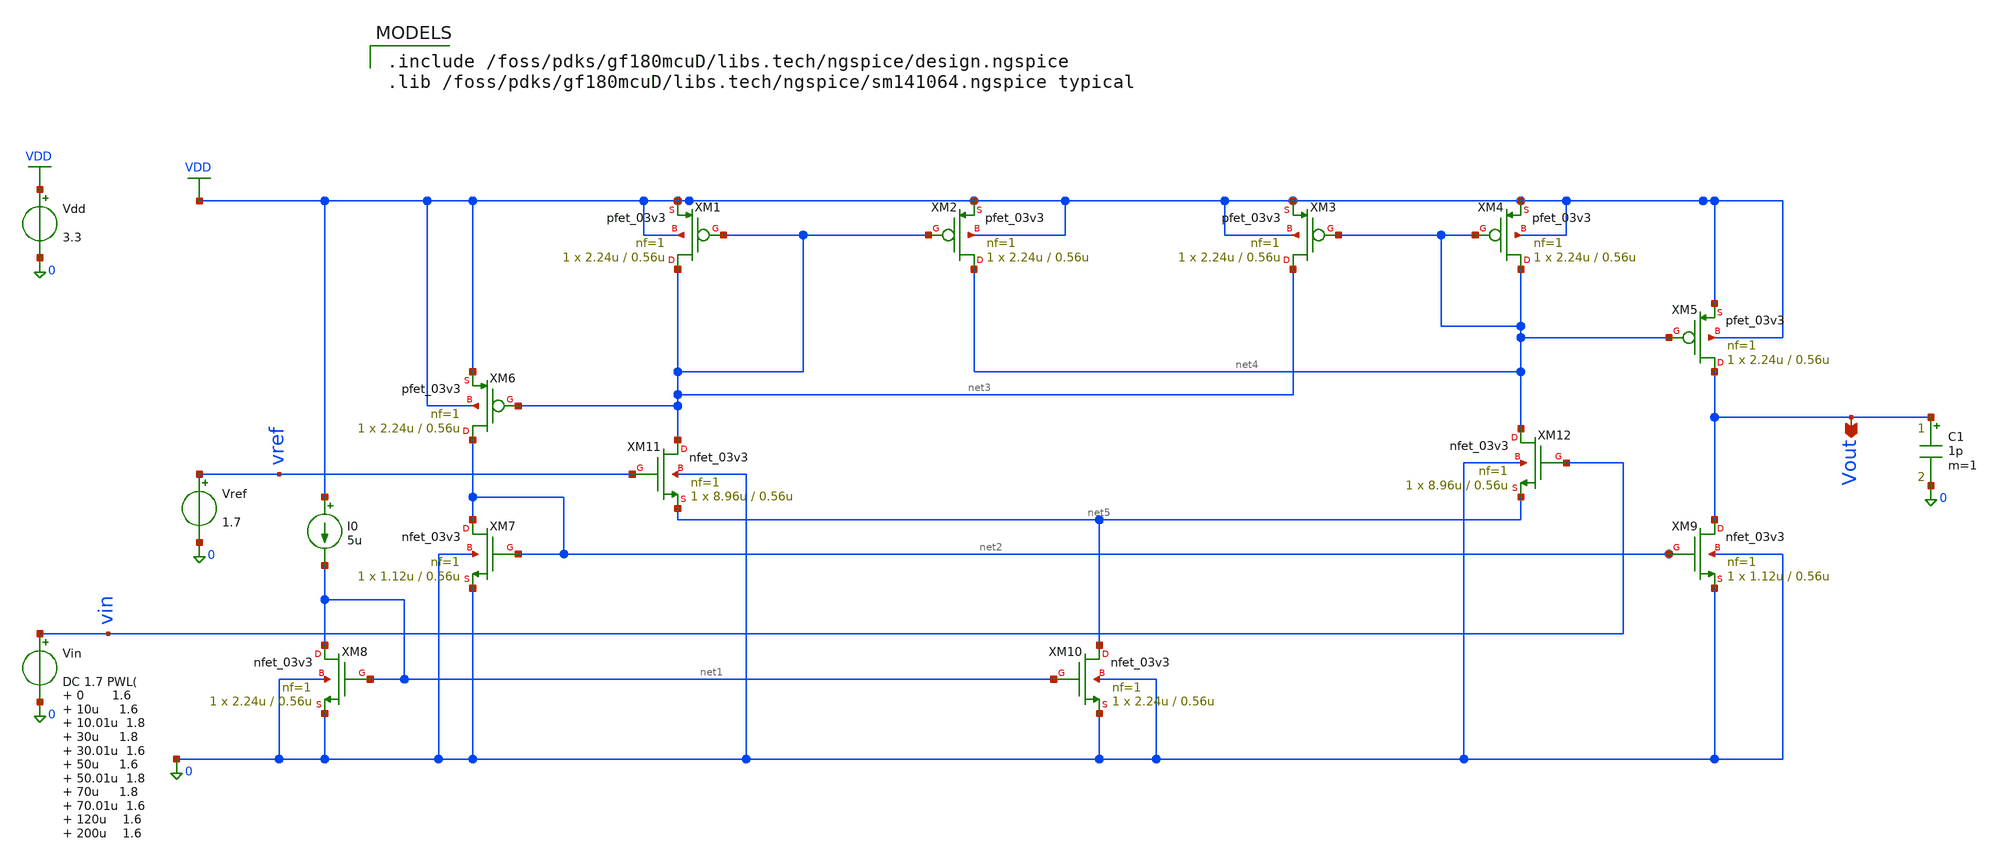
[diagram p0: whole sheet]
** sch_path: comparator/schematic-design/comparator_plot.sch
**.subckt comparator_plot Vout
*.opin Vout
XM1 net3 net3 VDD VDD pfet_03v3 L=0.56u W=2.24u nf=1 ad='int((nf+1)/2) * W/nf * 0.18u' as='int((nf+2)/2) * W/nf * 0.18u'
+ pd='2*int((nf+1)/2) * (W/nf + 0.18u)' ps='2*int((nf+2)/2) * (W/nf + 0.18u)' nrd='0.18u / W' nrs='0.18u / W'
+ sa=0 sb=0 sd=0 m=1
XM2 net4 net3 VDD VDD pfet_03v3 L=0.56u W=2.24u nf=1 ad='int((nf+1)/2) * W/nf * 0.18u' as='int((nf+2)/2) * W/nf * 0.18u'
+ pd='2*int((nf+1)/2) * (W/nf + 0.18u)' ps='2*int((nf+2)/2) * (W/nf + 0.18u)' nrd='0.18u / W' nrs='0.18u / W'
+ sa=0 sb=0 sd=0 m=1
XM3 net3 net4 VDD VDD pfet_03v3 L=0.56u W=2.24u nf=1 ad='int((nf+1)/2) * W/nf * 0.18u' as='int((nf+2)/2) * W/nf * 0.18u'
+ pd='2*int((nf+1)/2) * (W/nf + 0.18u)' ps='2*int((nf+2)/2) * (W/nf + 0.18u)' nrd='0.18u / W' nrs='0.18u / W'
+ sa=0 sb=0 sd=0 m=1
XM4 net4 net4 VDD VDD pfet_03v3 L=0.56u W=2.24u nf=1 ad='int((nf+1)/2) * W/nf * 0.18u' as='int((nf+2)/2) * W/nf * 0.18u'
+ pd='2*int((nf+1)/2) * (W/nf + 0.18u)' ps='2*int((nf+2)/2) * (W/nf + 0.18u)' nrd='0.18u / W' nrs='0.18u / W'
+ sa=0 sb=0 sd=0 m=1
XM5 Vout net4 VDD VDD pfet_03v3 L=0.56u W=2.24u nf=1 ad='int((nf+1)/2) * W/nf * 0.18u' as='int((nf+2)/2) * W/nf * 0.18u'
+ pd='2*int((nf+1)/2) * (W/nf + 0.18u)' ps='2*int((nf+2)/2) * (W/nf + 0.18u)' nrd='0.18u / W' nrs='0.18u / W'
+ sa=0 sb=0 sd=0 m=1
XM6 net2 net3 VDD VDD pfet_03v3 L=0.56u W=2.24u nf=1 ad='int((nf+1)/2) * W/nf * 0.18u' as='int((nf+2)/2) * W/nf * 0.18u'
+ pd='2*int((nf+1)/2) * (W/nf + 0.18u)' ps='2*int((nf+2)/2) * (W/nf + 0.18u)' nrd='0.18u / W' nrs='0.18u / W'
+ sa=0 sb=0 sd=0 m=1
XM7 net2 net2 0 0 nfet_03v3 L=0.56u W=1.12u nf=1 ad='int((nf+1)/2) * W/nf * 0.18u' as='int((nf+2)/2) * W/nf * 0.18u'
+ pd='2*int((nf+1)/2) * (W/nf + 0.18u)' ps='2*int((nf+2)/2) * (W/nf + 0.18u)' nrd='0.18u / W' nrs='0.18u / W'
+ sa=0 sb=0 sd=0 m=1
XM8 net1 net1 0 0 nfet_03v3 L=0.56u W=2.24u nf=1 ad='int((nf+1)/2) * W/nf * 0.18u' as='int((nf+2)/2) * W/nf * 0.18u'
+ pd='2*int((nf+1)/2) * (W/nf + 0.18u)' ps='2*int((nf+2)/2) * (W/nf + 0.18u)' nrd='0.18u / W' nrs='0.18u / W'
+ sa=0 sb=0 sd=0 m=1
XM9 Vout net2 0 0 nfet_03v3 L=0.56u W=1.12u nf=1 ad='int((nf+1)/2) * W/nf * 0.18u' as='int((nf+2)/2) * W/nf * 0.18u'
+ pd='2*int((nf+1)/2) * (W/nf + 0.18u)' ps='2*int((nf+2)/2) * (W/nf + 0.18u)' nrd='0.18u / W' nrs='0.18u / W'
+ sa=0 sb=0 sd=0 m=1
XM10 net5 net1 0 0 nfet_03v3 L=0.56u W=2.24u nf=1 ad='int((nf+1)/2) * W/nf * 0.18u' as='int((nf+2)/2) * W/nf * 0.18u'
+ pd='2*int((nf+1)/2) * (W/nf + 0.18u)' ps='2*int((nf+2)/2) * (W/nf + 0.18u)' nrd='0.18u / W' nrs='0.18u / W'
+ sa=0 sb=0 sd=0 m=1
XM11 net3 vref net5 0 nfet_03v3 L=0.56u W=8.96u nf=1 ad='int((nf+1)/2) * W/nf * 0.18u' as='int((nf+2)/2) * W/nf * 0.18u'
+ pd='2*int((nf+1)/2) * (W/nf + 0.18u)' ps='2*int((nf+2)/2) * (W/nf + 0.18u)' nrd='0.18u / W' nrs='0.18u / W'
+ sa=0 sb=0 sd=0 m=1
XM12 net4 vin net5 0 nfet_03v3 L=0.56u W=8.96u nf=1 ad='int((nf+1)/2) * W/nf * 0.18u' as='int((nf+2)/2) * W/nf * 0.18u'
+ pd='2*int((nf+1)/2) * (W/nf + 0.18u)' ps='2*int((nf+2)/2) * (W/nf + 0.18u)' nrd='0.18u / W' nrs='0.18u / W'
+ sa=0 sb=0 sd=0 m=1
I0 VDD net1 5u
Vref vref 0 1.7
Vin vin 0 DC 1.7 PWL( 0 1.6 10u 1.6 10.01u 1.8 30u 1.8 30.01u 1.6 50u 1.6 50.01u 1.8 70u 1.8 70.01u
+ 1.6 120u 1.6 200u 1.6 300u 1.8 400u 1.6 420u 1.6
)

Vdd VDD 0 3.3
C1 Vout 0 1p m=1
**** begin user architecture code

.include /foss/pdks/gf180mcuD/libs.tech/ngspice/design.ngspice
.lib /foss/pdks/gf180mcuD/libs.tech/ngspice/sm141064.ngspice typical


.control
set noaskquit
save v(vin) v(vref) v(vout) i(Vdd)

* ============================================================
* FIGURE 1 — DC TRANSFER / COMPARATOR SPECIFICATION
* Current design: VDD=3.3 V, VREF=1.7 V
* Sweep VIN around VREF. The output transition gives the trip point.
* ============================================================
set appendwrite
alter @Vin[dc] = 1.7
dc Vin 1.60 1.80 0.1m
meas dc vtrip_up find v(vin) when v(vout)=1.65 rise=1
write comparator_fig1_up.raw v(vin) v(vout)

reset
alter @Vin[dc] = 1.7
dc Vin 1.80 1.60 -0.1m
meas dc vtrip_down find v(vin) when v(vout)=1.65 fall=1
write comparator_fig1_down.raw v(vin) v(vout)

let vhyst_mV = abs(vtrip_up-vtrip_down)*1e3
let vcenter = (vtrip_up+vtrip_down)/2
let center_error_mV = (vcenter-1.7)*1e3
print vtrip_up vtrip_down vhyst_mV vcenter center_error_mV

* Open comparator_fig1_up.raw and comparator_fig1_down.raw together in
* Xschem's graph viewer to reproduce the two switching thresholds.
plot v(vout) vs v(vin) xlimit 1.60 1.80 ylimit -0.1 3.4

* ============================================================
* FIGURE 2 — TRANSIENT COMPARATOR RESPONSE
* Replaces VIN by a sine centered at 1.7 V. VOUT should become square.
* 0.2 V amplitude, 2 kHz, total time 4 ms.
* ============================================================
reset
alter @Vin[dc] = 1.7
alter @Vin[sin] = [ 1.7 0.2 2k 0 0 0 ]
tran 0.5u 4m
write comparator_fig2_tran.raw v(vin) v(vout)
plot v(vin) v(vout) xlimit 0 4m ylimit -0.1 3.4

* Propagation-delay measurements at VREF and VDD/2 output level
meas tran tpd_rise trig v(vin) val=1.7 rise=2 targ v(vout) val=1.65 rise=2
meas tran tpd_fall trig v(vin) val=1.7 fall=2 targ v(vout) val=1.65 fall=2
let tpd_rise_us=tpd_rise*1e6
let tpd_fall_us=tpd_fall*1e6
print tpd_rise_us tpd_fall_us

* ============================================================
* FIGURE 3 — VOLTAGE/TEMPERATURE OVERLAY FOR CURRENT PROCESS CORNER
* True TT/FF/SS must be run as separate netlists because .lib corner is
* chosen while ngspice parses the circuit. The shell script supplied with
* this file automates those three runs.
* ============================================================
reset
alter @Vin[pulse] = [ 1.60 1.80 50u 1n 1n 180u 360u ]
tran 0.1u 360u
write comparator_fig3_current_corner.raw v(vin) v(vout)
plot v(vin) v(vout) xlimit 0 360u ylimit -0.1 3.4
.endc


**** end user architecture code
**.ends
.GLOBAL VDD
.end
